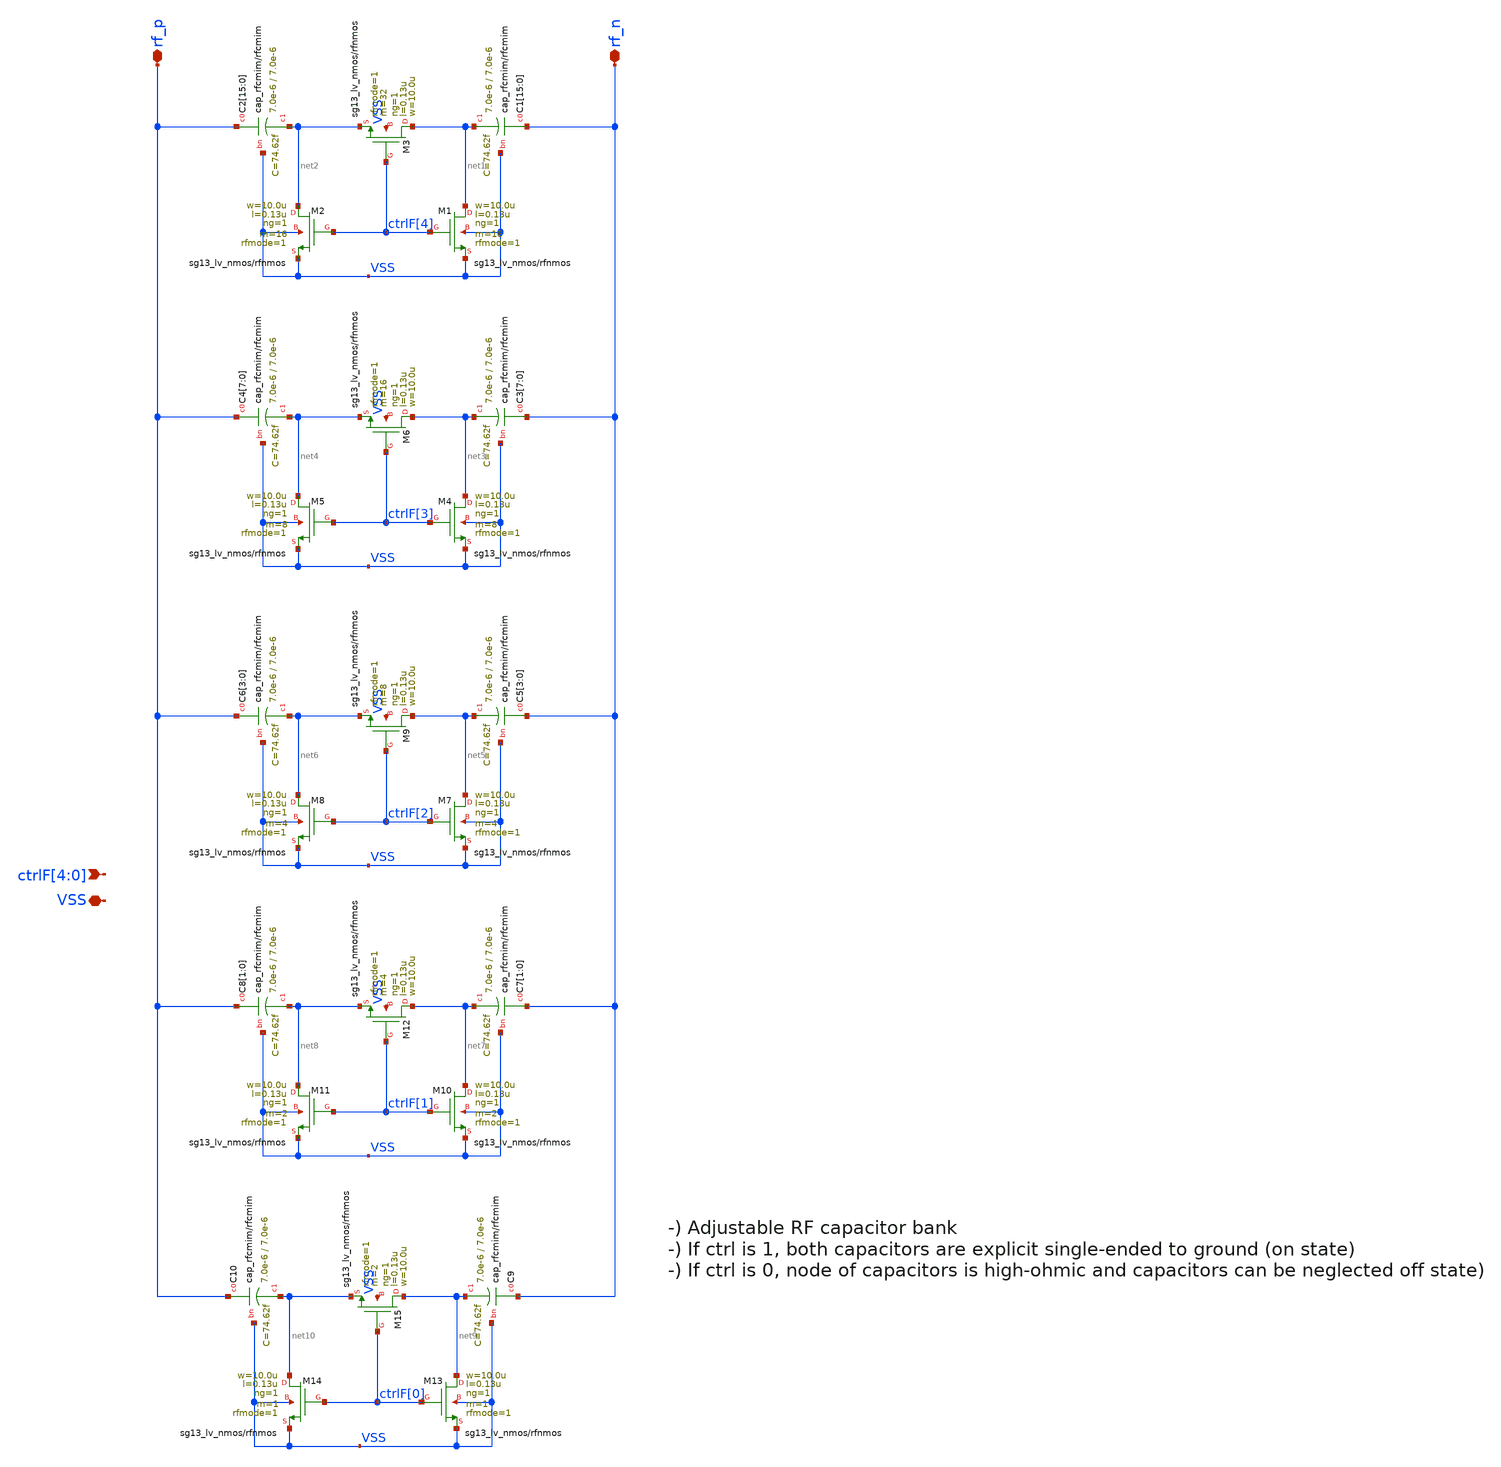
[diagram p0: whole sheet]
** sch_path: xschem/iruwbtx7_osci_capBank.sch
**.subckt iruwbtx7_osci_capBank ctrlF[4],ctrlF[3],ctrlF[2],ctrlF[1],ctrlF[0] VSS rf_p rf_n
*.ipin ctrlF[4],ctrlF[3],ctrlF[2],ctrlF[1],ctrlF[0]
*.iopin VSS
*.iopin rf_p
*.iopin rf_n
XC1[15] rf_n net1 VSS cap_rfcmim w=7.0e-6 l=7.0e-6 wfeed=1.0e-6 m=1 mm_ok=1
XC1[14] rf_n net1 VSS cap_rfcmim w=7.0e-6 l=7.0e-6 wfeed=1.0e-6 m=1 mm_ok=1
XC1[13] rf_n net1 VSS cap_rfcmim w=7.0e-6 l=7.0e-6 wfeed=1.0e-6 m=1 mm_ok=1
XC1[12] rf_n net1 VSS cap_rfcmim w=7.0e-6 l=7.0e-6 wfeed=1.0e-6 m=1 mm_ok=1
XC1[11] rf_n net1 VSS cap_rfcmim w=7.0e-6 l=7.0e-6 wfeed=1.0e-6 m=1 mm_ok=1
XC1[10] rf_n net1 VSS cap_rfcmim w=7.0e-6 l=7.0e-6 wfeed=1.0e-6 m=1 mm_ok=1
XC1[9] rf_n net1 VSS cap_rfcmim w=7.0e-6 l=7.0e-6 wfeed=1.0e-6 m=1 mm_ok=1
XC1[8] rf_n net1 VSS cap_rfcmim w=7.0e-6 l=7.0e-6 wfeed=1.0e-6 m=1 mm_ok=1
XC1[7] rf_n net1 VSS cap_rfcmim w=7.0e-6 l=7.0e-6 wfeed=1.0e-6 m=1 mm_ok=1
XC1[6] rf_n net1 VSS cap_rfcmim w=7.0e-6 l=7.0e-6 wfeed=1.0e-6 m=1 mm_ok=1
XC1[5] rf_n net1 VSS cap_rfcmim w=7.0e-6 l=7.0e-6 wfeed=1.0e-6 m=1 mm_ok=1
XC1[4] rf_n net1 VSS cap_rfcmim w=7.0e-6 l=7.0e-6 wfeed=1.0e-6 m=1 mm_ok=1
XC1[3] rf_n net1 VSS cap_rfcmim w=7.0e-6 l=7.0e-6 wfeed=1.0e-6 m=1 mm_ok=1
XC1[2] rf_n net1 VSS cap_rfcmim w=7.0e-6 l=7.0e-6 wfeed=1.0e-6 m=1 mm_ok=1
XC1[1] rf_n net1 VSS cap_rfcmim w=7.0e-6 l=7.0e-6 wfeed=1.0e-6 m=1 mm_ok=1
XC1[0] rf_n net1 VSS cap_rfcmim w=7.0e-6 l=7.0e-6 wfeed=1.0e-6 m=1 mm_ok=1
XM1 net1 ctrlF[4] VSS VSS sg13_lv_nmos w=10.0u l=0.13u ng=1 m=16 rfmode=1 mm_ok=1
XM2 net2 ctrlF[4] VSS VSS sg13_lv_nmos w=10.0u l=0.13u ng=1 m=16 rfmode=1 mm_ok=1
XM3 net1 ctrlF[4] net2 VSS sg13_lv_nmos w=10.0u l=0.13u ng=1 m=32 rfmode=1 mm_ok=1
XC2[15] rf_p net2 VSS cap_rfcmim w=7.0e-6 l=7.0e-6 wfeed=1.0e-6 m=1 mm_ok=1
XC2[14] rf_p net2 VSS cap_rfcmim w=7.0e-6 l=7.0e-6 wfeed=1.0e-6 m=1 mm_ok=1
XC2[13] rf_p net2 VSS cap_rfcmim w=7.0e-6 l=7.0e-6 wfeed=1.0e-6 m=1 mm_ok=1
XC2[12] rf_p net2 VSS cap_rfcmim w=7.0e-6 l=7.0e-6 wfeed=1.0e-6 m=1 mm_ok=1
XC2[11] rf_p net2 VSS cap_rfcmim w=7.0e-6 l=7.0e-6 wfeed=1.0e-6 m=1 mm_ok=1
XC2[10] rf_p net2 VSS cap_rfcmim w=7.0e-6 l=7.0e-6 wfeed=1.0e-6 m=1 mm_ok=1
XC2[9] rf_p net2 VSS cap_rfcmim w=7.0e-6 l=7.0e-6 wfeed=1.0e-6 m=1 mm_ok=1
XC2[8] rf_p net2 VSS cap_rfcmim w=7.0e-6 l=7.0e-6 wfeed=1.0e-6 m=1 mm_ok=1
XC2[7] rf_p net2 VSS cap_rfcmim w=7.0e-6 l=7.0e-6 wfeed=1.0e-6 m=1 mm_ok=1
XC2[6] rf_p net2 VSS cap_rfcmim w=7.0e-6 l=7.0e-6 wfeed=1.0e-6 m=1 mm_ok=1
XC2[5] rf_p net2 VSS cap_rfcmim w=7.0e-6 l=7.0e-6 wfeed=1.0e-6 m=1 mm_ok=1
XC2[4] rf_p net2 VSS cap_rfcmim w=7.0e-6 l=7.0e-6 wfeed=1.0e-6 m=1 mm_ok=1
XC2[3] rf_p net2 VSS cap_rfcmim w=7.0e-6 l=7.0e-6 wfeed=1.0e-6 m=1 mm_ok=1
XC2[2] rf_p net2 VSS cap_rfcmim w=7.0e-6 l=7.0e-6 wfeed=1.0e-6 m=1 mm_ok=1
XC2[1] rf_p net2 VSS cap_rfcmim w=7.0e-6 l=7.0e-6 wfeed=1.0e-6 m=1 mm_ok=1
XC2[0] rf_p net2 VSS cap_rfcmim w=7.0e-6 l=7.0e-6 wfeed=1.0e-6 m=1 mm_ok=1
XC3[7] rf_n net3 VSS cap_rfcmim w=7.0e-6 l=7.0e-6 wfeed=1.0e-6 m=1 mm_ok=1
XC3[6] rf_n net3 VSS cap_rfcmim w=7.0e-6 l=7.0e-6 wfeed=1.0e-6 m=1 mm_ok=1
XC3[5] rf_n net3 VSS cap_rfcmim w=7.0e-6 l=7.0e-6 wfeed=1.0e-6 m=1 mm_ok=1
XC3[4] rf_n net3 VSS cap_rfcmim w=7.0e-6 l=7.0e-6 wfeed=1.0e-6 m=1 mm_ok=1
XC3[3] rf_n net3 VSS cap_rfcmim w=7.0e-6 l=7.0e-6 wfeed=1.0e-6 m=1 mm_ok=1
XC3[2] rf_n net3 VSS cap_rfcmim w=7.0e-6 l=7.0e-6 wfeed=1.0e-6 m=1 mm_ok=1
XC3[1] rf_n net3 VSS cap_rfcmim w=7.0e-6 l=7.0e-6 wfeed=1.0e-6 m=1 mm_ok=1
XC3[0] rf_n net3 VSS cap_rfcmim w=7.0e-6 l=7.0e-6 wfeed=1.0e-6 m=1 mm_ok=1
XM4 net3 ctrlF[3] VSS VSS sg13_lv_nmos w=10.0u l=0.13u ng=1 m=8 rfmode=1 mm_ok=1
XM5 net4 ctrlF[3] VSS VSS sg13_lv_nmos w=10.0u l=0.13u ng=1 m=8 rfmode=1 mm_ok=1
XM6 net3 ctrlF[3] net4 VSS sg13_lv_nmos w=10.0u l=0.13u ng=1 m=16 rfmode=1 mm_ok=1
XC4[7] rf_p net4 VSS cap_rfcmim w=7.0e-6 l=7.0e-6 wfeed=1.0e-6 m=1 mm_ok=1
XC4[6] rf_p net4 VSS cap_rfcmim w=7.0e-6 l=7.0e-6 wfeed=1.0e-6 m=1 mm_ok=1
XC4[5] rf_p net4 VSS cap_rfcmim w=7.0e-6 l=7.0e-6 wfeed=1.0e-6 m=1 mm_ok=1
XC4[4] rf_p net4 VSS cap_rfcmim w=7.0e-6 l=7.0e-6 wfeed=1.0e-6 m=1 mm_ok=1
XC4[3] rf_p net4 VSS cap_rfcmim w=7.0e-6 l=7.0e-6 wfeed=1.0e-6 m=1 mm_ok=1
XC4[2] rf_p net4 VSS cap_rfcmim w=7.0e-6 l=7.0e-6 wfeed=1.0e-6 m=1 mm_ok=1
XC4[1] rf_p net4 VSS cap_rfcmim w=7.0e-6 l=7.0e-6 wfeed=1.0e-6 m=1 mm_ok=1
XC4[0] rf_p net4 VSS cap_rfcmim w=7.0e-6 l=7.0e-6 wfeed=1.0e-6 m=1 mm_ok=1
XC5[3] rf_n net5 VSS cap_rfcmim w=7.0e-6 l=7.0e-6 wfeed=1.0e-6 m=1 mm_ok=1
XC5[2] rf_n net5 VSS cap_rfcmim w=7.0e-6 l=7.0e-6 wfeed=1.0e-6 m=1 mm_ok=1
XC5[1] rf_n net5 VSS cap_rfcmim w=7.0e-6 l=7.0e-6 wfeed=1.0e-6 m=1 mm_ok=1
XC5[0] rf_n net5 VSS cap_rfcmim w=7.0e-6 l=7.0e-6 wfeed=1.0e-6 m=1 mm_ok=1
XM7 net5 ctrlF[2] VSS VSS sg13_lv_nmos w=10.0u l=0.13u ng=1 m=4 rfmode=1 mm_ok=1
XM8 net6 ctrlF[2] VSS VSS sg13_lv_nmos w=10.0u l=0.13u ng=1 m=4 rfmode=1 mm_ok=1
XM9 net5 ctrlF[2] net6 VSS sg13_lv_nmos w=10.0u l=0.13u ng=1 m=8 rfmode=1 mm_ok=1
XC6[3] rf_p net6 VSS cap_rfcmim w=7.0e-6 l=7.0e-6 wfeed=1.0e-6 m=1 mm_ok=1
XC6[2] rf_p net6 VSS cap_rfcmim w=7.0e-6 l=7.0e-6 wfeed=1.0e-6 m=1 mm_ok=1
XC6[1] rf_p net6 VSS cap_rfcmim w=7.0e-6 l=7.0e-6 wfeed=1.0e-6 m=1 mm_ok=1
XC6[0] rf_p net6 VSS cap_rfcmim w=7.0e-6 l=7.0e-6 wfeed=1.0e-6 m=1 mm_ok=1
XC7[1] rf_n net7 VSS cap_rfcmim w=7.0e-6 l=7.0e-6 wfeed=1.0e-6 m=1 mm_ok=1
XC7[0] rf_n net7 VSS cap_rfcmim w=7.0e-6 l=7.0e-6 wfeed=1.0e-6 m=1 mm_ok=1
XM10 net7 ctrlF[1] VSS VSS sg13_lv_nmos w=10.0u l=0.13u ng=1 m=2 rfmode=1 mm_ok=1
XM11 net8 ctrlF[1] VSS VSS sg13_lv_nmos w=10.0u l=0.13u ng=1 m=2 rfmode=1 mm_ok=1
XM12 net7 ctrlF[1] net8 VSS sg13_lv_nmos w=10.0u l=0.13u ng=1 m=4 rfmode=1 mm_ok=1
XC8[1] rf_p net8 VSS cap_rfcmim w=7.0e-6 l=7.0e-6 wfeed=1.0e-6 m=1 mm_ok=1
XC8[0] rf_p net8 VSS cap_rfcmim w=7.0e-6 l=7.0e-6 wfeed=1.0e-6 m=1 mm_ok=1
XC9 rf_n net9 VSS cap_rfcmim w=7.0e-6 l=7.0e-6 wfeed=1.0e-6 m=1 mm_ok=1
XM13 net9 ctrlF[0] VSS VSS sg13_lv_nmos w=10.0u l=0.13u ng=1 m=1 rfmode=1 mm_ok=1
XM14 net10 ctrlF[0] VSS VSS sg13_lv_nmos w=10.0u l=0.13u ng=1 m=1 rfmode=1 mm_ok=1
XM15 net9 ctrlF[0] net10 VSS sg13_lv_nmos w=10.0u l=0.13u ng=1 m=2 rfmode=1 mm_ok=1
XC10 rf_p net10 VSS cap_rfcmim w=7.0e-6 l=7.0e-6 wfeed=1.0e-6 m=1 mm_ok=1
**.ends
.end
